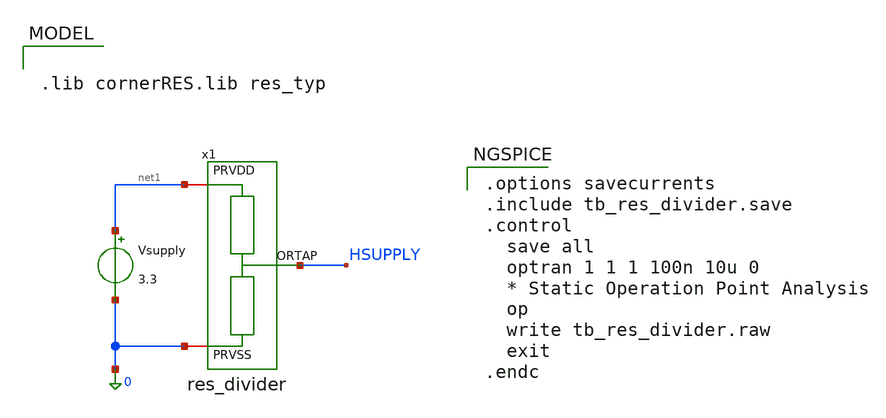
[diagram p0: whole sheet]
** sch_path: xschem/tb_res_divider.sch
**.subckt tb_res_divider
Vsupply net1 0 3.3
x1 net1 HSUPPLY 0 res_divider
**** begin user architecture code

.options savecurrents
.include tb_res_divider.save
.control
  save all
  optran 1 1 1 100n 10u 0
  * Static Operation Point Analysis
  op
  write tb_res_divider.raw
  exit
.endc




.lib cornerRES.lib res_typ


**** end user architecture code
**.ends

* expanding   symbol:  res_divider.sym # of pins=3
** sym_path: xschem/res_divider.sym
** sch_path: xschem/res_divider.sch
.subckt res_divider PRVDD ORTAP PRVSS
*.iopin PRVDD
*.iopin PRVSS
*.opin ORTAP
XR1 PRVSS ORTAP PRVSS rhigh w=0.5e-6 l=298e-6 m=1 b=2 mm_ok=1
XR2 ORTAP PRVDD PRVSS rhigh w=0.5e-6 l=298e-6 m=1 b=2 mm_ok=1
.ends

.end
